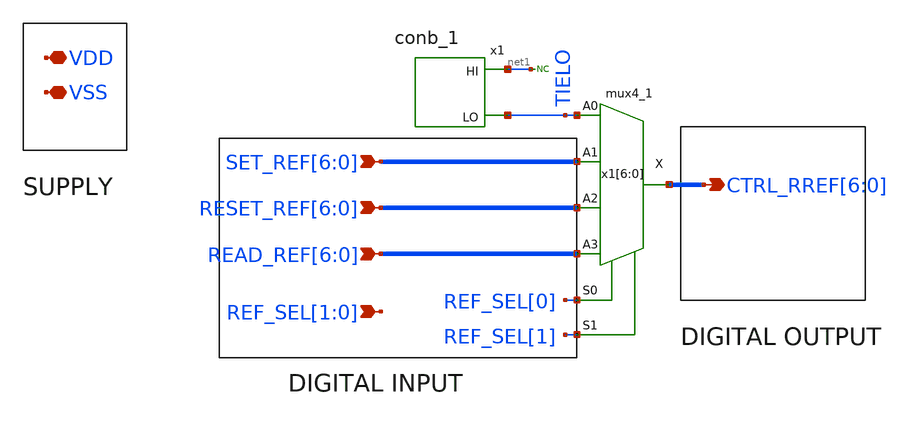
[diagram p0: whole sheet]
** sch_path: BL_Read_Interface/rram_read_csa_refmux.sch
**.subckt rram_read_csa_refmux
*+ SET_REF[6],SET_REF[5],SET_REF[4],SET_REF[3],SET_REF[2],SET_REF[1],SET_REF[0] RESET_REF[6],RESET_REF[5],RESET_REF[4],RESET_REF[3],RESET_REF[2],RESET_REF[1],RESET_REF[0]
*+ READ_REF[6],READ_REF[5],READ_REF[4],READ_REF[3],READ_REF[2],READ_REF[1],READ_REF[0] REF_SEL[1],REF_SEL[0]
*+ CTRL_RREF[6],CTRL_RREF[5],CTRL_RREF[4],CTRL_RREF[3],CTRL_RREF[2],CTRL_RREF[1],CTRL_RREF[0] VDD VSS
*.ipin SET_REF[6],SET_REF[5],SET_REF[4],SET_REF[3],SET_REF[2],SET_REF[1],SET_REF[0]
*.ipin RESET_REF[6],RESET_REF[5],RESET_REF[4],RESET_REF[3],RESET_REF[2],RESET_REF[1],RESET_REF[0]
*.ipin READ_REF[6],READ_REF[5],READ_REF[4],READ_REF[3],READ_REF[2],READ_REF[1],READ_REF[0]
*.ipin REF_SEL[1],REF_SEL[0]
*.opin CTRL_RREF[6],CTRL_RREF[5],CTRL_RREF[4],CTRL_RREF[3],CTRL_RREF[2],CTRL_RREF[1],CTRL_RREF[0]
*.iopin VDD
*.iopin VSS
x1[6] TIELO SET_REF[6] RESET_REF[6] READ_REF[6] REF_SEL[0] REF_SEL[1] VSS VSS VDD VDD CTRL_RREF[6]
+ sky130_fd_sc_hd__mux4_1
x1[5] TIELO SET_REF[5] RESET_REF[5] READ_REF[5] REF_SEL[0] REF_SEL[1] VSS VSS VDD VDD CTRL_RREF[5]
+ sky130_fd_sc_hd__mux4_1
x1[4] TIELO SET_REF[4] RESET_REF[4] READ_REF[4] REF_SEL[0] REF_SEL[1] VSS VSS VDD VDD CTRL_RREF[4]
+ sky130_fd_sc_hd__mux4_1
x1[3] TIELO SET_REF[3] RESET_REF[3] READ_REF[3] REF_SEL[0] REF_SEL[1] VSS VSS VDD VDD CTRL_RREF[3]
+ sky130_fd_sc_hd__mux4_1
x1[2] TIELO SET_REF[2] RESET_REF[2] READ_REF[2] REF_SEL[0] REF_SEL[1] VSS VSS VDD VDD CTRL_RREF[2]
+ sky130_fd_sc_hd__mux4_1
x1[1] TIELO SET_REF[1] RESET_REF[1] READ_REF[1] REF_SEL[0] REF_SEL[1] VSS VSS VDD VDD CTRL_RREF[1]
+ sky130_fd_sc_hd__mux4_1
x1[0] TIELO SET_REF[0] RESET_REF[0] READ_REF[0] REF_SEL[0] REF_SEL[1] VSS VSS VDD VDD CTRL_RREF[0]
+ sky130_fd_sc_hd__mux4_1
x1 VSS VSS VDD VDD net1 TIELO sky130_fd_sc_hd__conb_1
* noconn #net1
**.ends
.end
